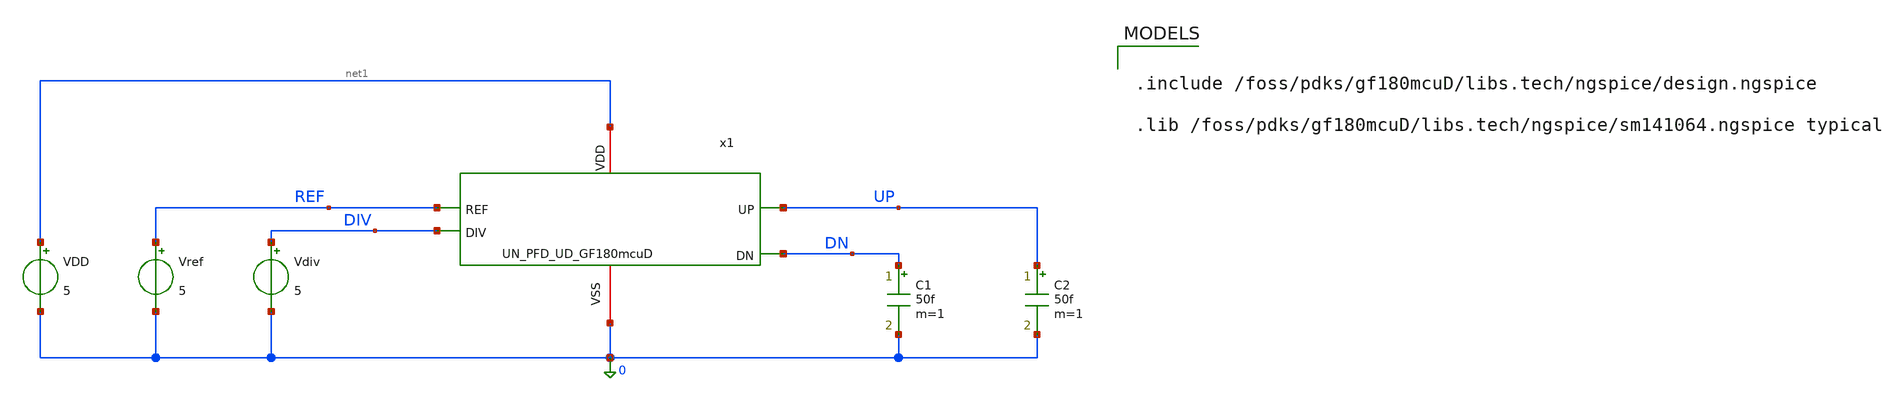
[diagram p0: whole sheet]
** sch_path: src/UN_PFD_GF180mcuD/work/UN_PFD_UD_GF180mcuD_TB.sch
**.subckt UN_PFD_UD_GF180mcuD_TB
x1 net1 UP REF 0 DIV DN UN_PFD_UD_GF180mcuD
Vref REF 0 5
Vdiv DIV 0 5
VDD net1 0 5
C1 DN 0 50f m=1
C2 UP 0 50f m=1
**** begin user architecture code

.include /foss/pdks/gf180mcuD/libs.tech/ngspice/design.ngspice

.lib /foss/pdks/gf180mcuD/libs.tech/ngspice/sm141064.ngspice typical




.control
save all
set filetype=ascii

.include /foss/designs/UN_BasicPLL_GF180mcuD/UN_PFD_GF180mcuD/gf180dffrnq_1.spice
.include /foss/designs/UN_BasicPLL_GF180mcuD/UN_PFD_GF180mcuD/gf180nand2.spice

** Define Input Signal Properties.
** let allows calculations. set does not.

let fsig = 0.1e7
let tper = 1/fsig
let tfr = 0.01*tper
let ton = 0.5*tper-2*tfr
let tdel= 0.2*tper

** Define the parameters for Transient Analysis
** For transient Analysis, you have 2 parameters typically, How long to run sim and step size.

let tstop = 5*tper
let tstep = 0.001*tper

** Set the input sources with these parameters.
** VDD is already stable, but you can choose to simulate it separately.
** You use alter command to edit the default properties of the sources

alter @Vref[DC] = 0.0
alter @Vdiv[DC] = 5
alter @Vref[PULSE] = [ 0 5 0 $&tfr $&tfr $&ton $&tper ]
alter @Vdiv[PULSE] = [ 0 5 $&tdel $&tfr $&tfr $&ton $&tper ]

**** list of simulations to perform
**** The $& evaluates expressions and converts results to string because parameters are expected to
*+ be string

op
tran $&tstep $&tstop

** plots
setplot tran1
let vup = v(up)
let vdn = v(dn)
let vref= v(ref)
let vdiv= v(div)

let ivdd = vdd#branch *1e3 * -1

plot vup vdn vref vdiv

setplot op1

write /foss/designs/un_basicpll_gf180mcud/un_pfd_gf180mcud/sim/pfd_ud_tb.raw tran1.all

.endc


only_toplevel=true
**** end user architecture code
**.ends

* expanding   symbol:
*+  /foss/designs/UN_BasicPLL_GF180mcuD/UN_PFD_GF180mcuD/work/UN_PFD_UD_GF180mcuD.sym # of pins=6
** sym_path: src/UN_PFD_GF180mcuD/work/UN_PFD_UD_GF180mcuD.sym
** sch_path: src/UN_PFD_GF180mcuD/work/UN_PFD_UD_GF180mcuD.sch
.subckt UN_PFD_UD_GF180mcuD VDD UP REF VSS DIV DN
*.ipin REF
*.ipin DIV
*.iopin VDD
*.iopin VSS
*.opin UP
*.opin DN
dff1 VDD VDD net1 VSS UP REF VSS VDD UN_DFFRNQ_1_GF180mcuD
dff2 VDD VDD net1 net2 DN net3 net4 VDD UN_DFFRNQ_1_GF180mcuD
x1 DN UP net5 VDD net6 net7 net1 UN_NAND2_0_GF180mcuD
.ends

.end
